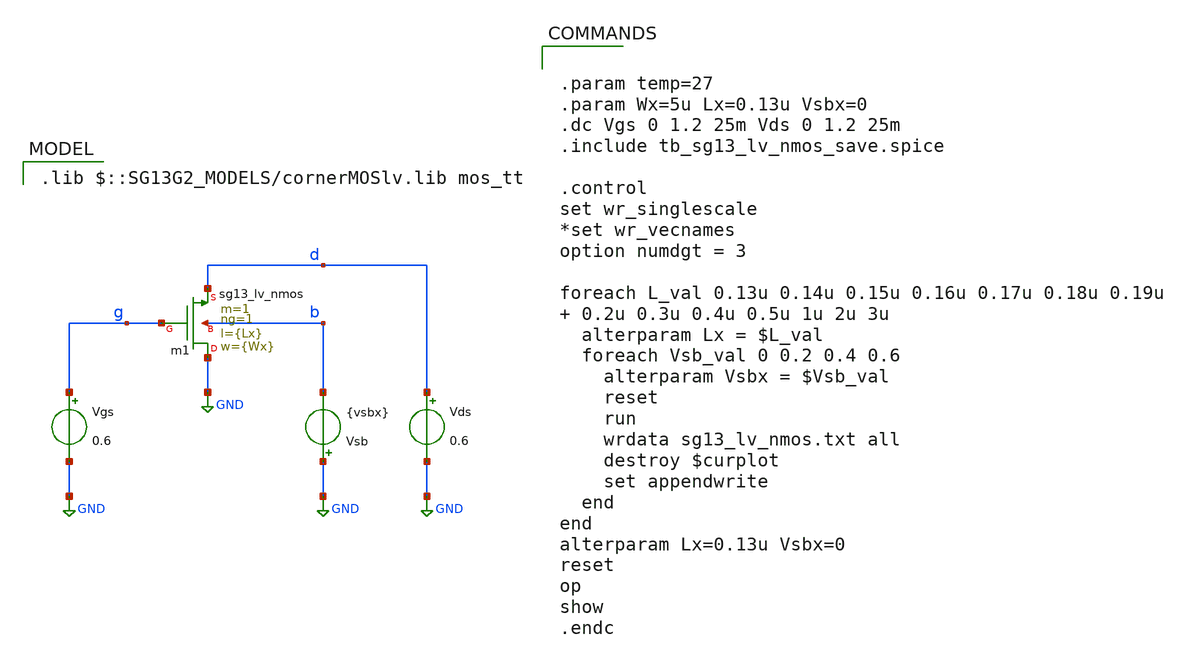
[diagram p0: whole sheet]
** sch_path: 4_Technology/src/tb_sg13_lv_nmos.sch
**.subckt tb_sg13_lv_nmos
Xm1 GND g d b sg13_lv_nmos w={Wx} l={Lx} ng=1 m=1 mm_ok=1
Vgs g GND 0.6
Vds d GND 0.6
Vsb GND b {vsbx}
**** begin user architecture code
 .lib $::SG13G2_MODELS/cornerMOSlv.lib mos_tt



.param temp=27
.param Wx=5u Lx=0.13u Vsbx=0
.dc Vgs 0 1.2 25m Vds 0 1.2 25m
.include tb_sg13_lv_nmos_save.spice

.control
set wr_singlescale
*set wr_vecnames
option numdgt = 3

foreach L_val 0.13u 0.14u 0.15u 0.16u 0.17u 0.18u 0.19u  0.2u 0.3u 0.4u 0.5u 1u 2u 3u
  alterparam Lx = $L_val
  foreach Vsb_val 0 0.2 0.4 0.6
    alterparam Vsbx = $Vsb_val
    reset
    run
    wrdata sg13_lv_nmos.txt all
    destroy $curplot
    set appendwrite
  end
end
alterparam Lx=0.13u Vsbx=0
reset
op
show
.endc


**** end user architecture code
**.ends
.GLOBAL GND
.end
